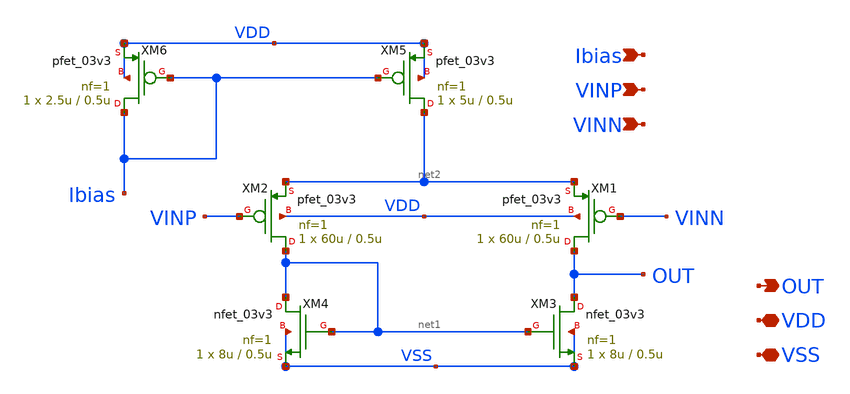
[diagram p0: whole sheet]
** sch_path: week02_current_diffpair/tugas5_cascode_current_mirror/p-5t-ota.sch
**.subckt p-5t-ota Ibias VINP VINN OUT VDD VSS
*.ipin Ibias
*.ipin VINP
*.ipin VINN
*.opin OUT
*.iopin VDD
*.iopin VSS
XM1 OUT VINN net2 VDD pfet_03v3 L=0.5u W=60u nf=1 ad='int((nf+1)/2) * W/nf * 0.18u' as='int((nf+2)/2) * W/nf * 0.18u'
+ pd='2*int((nf+1)/2) * (W/nf + 0.18u)' ps='2*int((nf+2)/2) * (W/nf + 0.18u)' nrd='0.18u / W' nrs='0.18u / W'
+ sa=0 sb=0 sd=0 m=1
XM2 net1 VINP net2 VDD pfet_03v3 L=0.5u W=60u nf=1 ad='int((nf+1)/2) * W/nf * 0.18u' as='int((nf+2)/2) * W/nf * 0.18u'
+ pd='2*int((nf+1)/2) * (W/nf + 0.18u)' ps='2*int((nf+2)/2) * (W/nf + 0.18u)' nrd='0.18u / W' nrs='0.18u / W'
+ sa=0 sb=0 sd=0 m=1
XM3 OUT net1 VSS VSS nfet_03v3 L=0.5u W=8u nf=1 ad='int((nf+1)/2) * W/nf * 0.18u' as='int((nf+2)/2) * W/nf * 0.18u'
+ pd='2*int((nf+1)/2) * (W/nf + 0.18u)' ps='2*int((nf+2)/2) * (W/nf + 0.18u)' nrd='0.18u / W' nrs='0.18u / W'
+ sa=0 sb=0 sd=0 m=1
XM4 net1 net1 VSS VSS nfet_03v3 L=0.5u W=8u nf=1 ad='int((nf+1)/2) * W/nf * 0.18u' as='int((nf+2)/2) * W/nf * 0.18u'
+ pd='2*int((nf+1)/2) * (W/nf + 0.18u)' ps='2*int((nf+2)/2) * (W/nf + 0.18u)' nrd='0.18u / W' nrs='0.18u / W'
+ sa=0 sb=0 sd=0 m=1
XM5 net2 Ibias VDD VDD pfet_03v3 L=0.5u W=5u nf=1 ad='int((nf+1)/2) * W/nf * 0.18u' as='int((nf+2)/2) * W/nf * 0.18u'
+ pd='2*int((nf+1)/2) * (W/nf + 0.18u)' ps='2*int((nf+2)/2) * (W/nf + 0.18u)' nrd='0.18u / W' nrs='0.18u / W'
+ sa=0 sb=0 sd=0 m=1
XM6 Ibias Ibias VDD VDD pfet_03v3 L=0.5u W=2.5u nf=1 ad='int((nf+1)/2) * W/nf * 0.18u' as='int((nf+2)/2) * W/nf * 0.18u'
+ pd='2*int((nf+1)/2) * (W/nf + 0.18u)' ps='2*int((nf+2)/2) * (W/nf + 0.18u)' nrd='0.18u / W' nrs='0.18u / W'
+ sa=0 sb=0 sd=0 m=1
**.ends
.end
